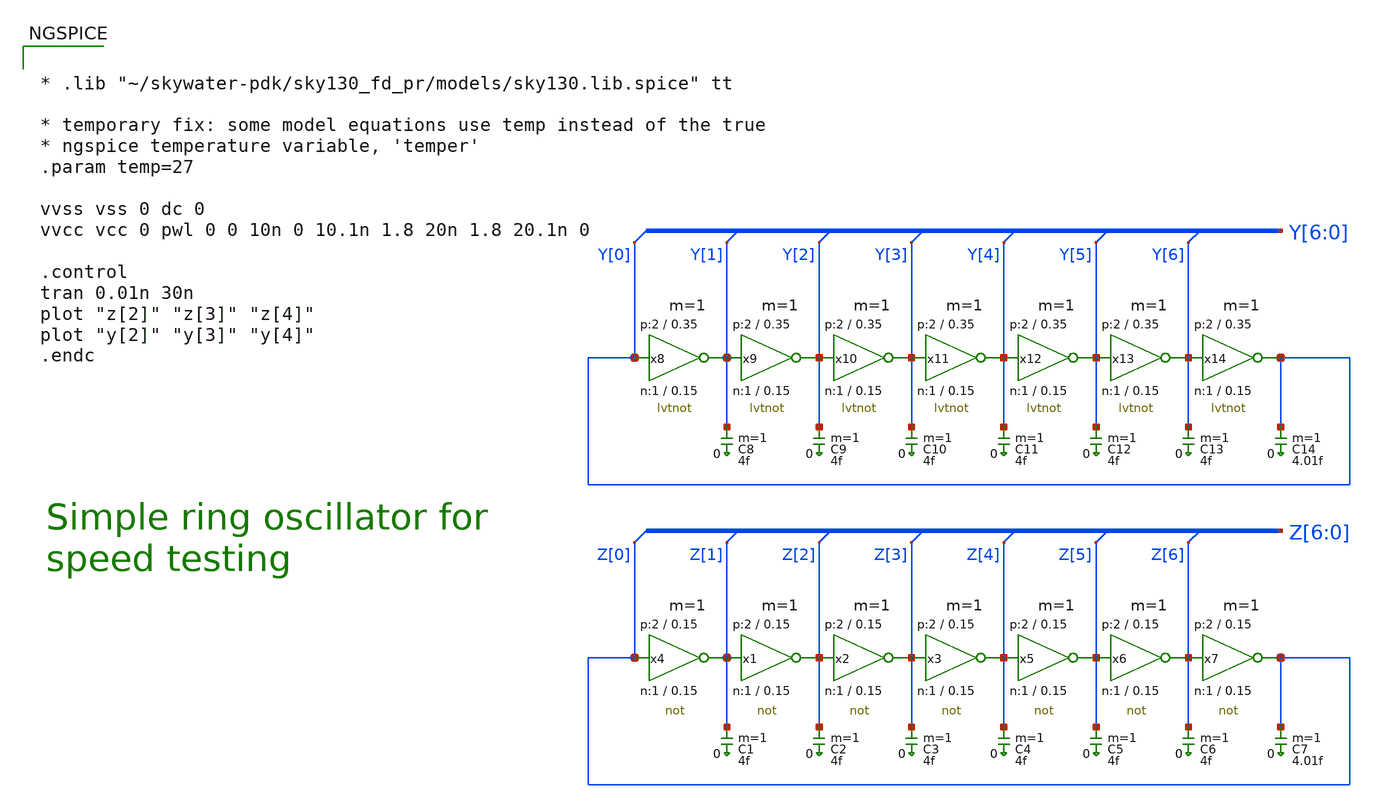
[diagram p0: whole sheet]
** sch_path: sky130_tests/test_inv.sch
* Copyright 2020 Stefan Frederik Schippers
* Licensed under the Apache License, Version 2.0 (the "License");
* you may not use this file except in compliance with the License.
* You may obtain a copy of the License at
* https://www.apache.org/licenses/LICENSE-2.0
* Unless required by applicable law or agreed to in writing, software
* distributed under the License is distributed on an "AS IS" BASIS,
* WITHOUT WARRANTIES OR CONDITIONS OF ANY KIND, either express or implied.
* See the License for the specific language governing permissions and
* limitations under the License.
**.subckt test_inv
x4 Z[1] Z[0] VCC VSS not W_N=1 L_N=0.15 W_P=2 L_P=0.15 m=1
C1 Z[1] 0 4f m=1
x1 Z[2] Z[1] VCC VSS not W_N=1 L_N=0.15 W_P=2 L_P=0.15 m=1
x2 Z[3] Z[2] VCC VSS not W_N=1 L_N=0.15 W_P=2 L_P=0.15 m=1
x3 Z[4] Z[3] VCC VSS not W_N=1 L_N=0.15 W_P=2 L_P=0.15 m=1
x5 Z[5] Z[4] VCC VSS not W_N=1 L_N=0.15 W_P=2 L_P=0.15 m=1
x6 Z[6] Z[5] VCC VSS not W_N=1 L_N=0.15 W_P=2 L_P=0.15 m=1
x7 Z[0] Z[6] VCC VSS not W_N=1 L_N=0.15 W_P=2 L_P=0.15 m=1
C2 Z[2] 0 4f m=1
C3 Z[3] 0 4f m=1
C4 Z[4] 0 4f m=1
C5 Z[5] 0 4f m=1
C6 Z[6] 0 4f m=1
C7 Z[0] 0 4.01f m=1
x8 Y[1] Y[0] VCC VSS lvtnot W_N=1 L_N=0.15 W_P=2 L_P=0.35 m=1
C8 Y[1] 0 4f m=1
x9 Y[2] Y[1] VCC VSS lvtnot W_N=1 L_N=0.15 W_P=2 L_P=0.35 m=1
x10 Y[3] Y[2] VCC VSS lvtnot W_N=1 L_N=0.15 W_P=2 L_P=0.35 m=1
x11 Y[4] Y[3] VCC VSS lvtnot W_N=1 L_N=0.15 W_P=2 L_P=0.35 m=1
x12 Y[5] Y[4] VCC VSS lvtnot W_N=1 L_N=0.15 W_P=2 L_P=0.35 m=1
x13 Y[6] Y[5] VCC VSS lvtnot W_N=1 L_N=0.15 W_P=2 L_P=0.35 m=1
x14 Y[0] Y[6] VCC VSS lvtnot W_N=1 L_N=0.15 W_P=2 L_P=0.35 m=1
C9 Y[2] 0 4f m=1
C10 Y[3] 0 4f m=1
C11 Y[4] 0 4f m=1
C12 Y[5] 0 4f m=1
C13 Y[6] 0 4f m=1
C14 Y[0] 0 4.01f m=1
**** begin user architecture code


* .lib "~/skywater-pdk/sky130_fd_pr/models/sky130.lib.spice" tt

* temporary fix: some model equations use temp instead of the true
* ngspice temperature variable, 'temper'
.param temp=27

vvss vss 0 dc 0
vvcc vcc 0 pwl 0 0 10n 0 10.1n 1.8 20n 1.8 20.1n 0

.control
tran 0.01n 30n
plot "z[2]" "z[3]" "z[4]"
plot "y[2]" "y[3]" "y[4]"
.endc


**** end user architecture code
**.ends
**** begin user architecture code

.include   ~/skywater-pdk/sky130_fd_pr_ngspice/cells/nfet_01v8/sky130_fd_pr__nfet_01v8__tt.corner.spice
.include ~/skywater-pdk/sky130_fd_pr_ngspice/cells/nfet_01v8_lvt/sky130_fd_pr__nfet_01v8_lvt__tt.corner.spice
.include ~/skywater-pdk/sky130_fd_pr_ngspice/cells/pfet_01v8/sky130_fd_pr__pfet_01v8__tt.corner.spice
.include ~/skywater-pdk/sky130_fd_pr_ngspice/cells/nfet_03v3_nvt/sky130_fd_pr__nfet_03v3_nvt__tt.corner.spice
.include ~/skywater-pdk/sky130_fd_pr_ngspice/cells/nfet_05v0_nvt/sky130_fd_pr__nfet_05v0_nvt__tt.corner.spice
.include ~/skywater-pdk/sky130_fd_pr_ngspice/cells/esd_nfet_01v8/sky130_fd_pr__esd_nfet_01v8__tt.corner.spice
.include ~/skywater-pdk/sky130_fd_pr_ngspice/cells/pfet_01v8_lvt/sky130_fd_pr__pfet_01v8_lvt__tt.corner.spice
.include ~/skywater-pdk/sky130_fd_pr_ngspice/cells/pfet_01v8_hvt/sky130_fd_pr__pfet_01v8_hvt__tt.corner.spice
.include ~/skywater-pdk/sky130_fd_pr_ngspice/cells/esd_pfet_g5v0d10v5/sky130_fd_pr__esd_pfet_g5v0d10v5__tt.corner.spice
.include ~/skywater-pdk/sky130_fd_pr_ngspice/cells/pfet_g5v0d10v5/sky130_fd_pr__pfet_g5v0d10v5__tt.corner.spice
.include ~/skywater-pdk/sky130_fd_pr_ngspice/cells/pfet_g5v0d16v0/sky130_fd_pr__pfet_g5v0d16v0__tt.corner.spice
.include ~/skywater-pdk/sky130_fd_pr_ngspice/cells/nfet_g5v0d10v5/sky130_fd_pr__nfet_g5v0d10v5__tt.corner.spice
.include ~/skywater-pdk/sky130_fd_pr_ngspice/cells/nfet_g5v0d16v0/sky130_fd_pr__nfet_g5v0d16v0__tt_discrete.corner.spice
.include ~/skywater-pdk/sky130_fd_pr_ngspice/cells/esd_nfet_g5v0d10v5/sky130_fd_pr__esd_nfet_g5v0d10v5__tt.corner.spice
.include ~/skywater-pdk/sky130_fd_pr_ngspice/models/corners/tt/nonfet.spice
* Mismatch parameters
.include ~/skywater-pdk/sky130_fd_pr_ngspice/cells/nfet_01v8/sky130_fd_pr__nfet_01v8__mismatch.corner.spice
.include ~/skywater-pdk/sky130_fd_pr_ngspice/cells/pfet_01v8/sky130_fd_pr__pfet_01v8__mismatch.corner.spice
.include ~/skywater-pdk/sky130_fd_pr_ngspice/cells/nfet_01v8_lvt/sky130_fd_pr__nfet_01v8_lvt__mismatch.corner.spice
.include ~/skywater-pdk/sky130_fd_pr_ngspice/cells/pfet_01v8_lvt/sky130_fd_pr__pfet_01v8_lvt__mismatch.corner.spice
.include ~/skywater-pdk/sky130_fd_pr_ngspice/cells/pfet_01v8_hvt/sky130_fd_pr__pfet_01v8_hvt__mismatch.corner.spice
.include ~/skywater-pdk/sky130_fd_pr_ngspice/cells/nfet_g5v0d10v5/sky130_fd_pr__nfet_g5v0d10v5__mismatch.corner.spice
.include ~/skywater-pdk/sky130_fd_pr_ngspice/cells/pfet_g5v0d10v5/sky130_fd_pr__pfet_g5v0d10v5__mismatch.corner.spice
.include ~/skywater-pdk/sky130_fd_pr_ngspice/cells/nfet_05v0_nvt/sky130_fd_pr__nfet_05v0_nvt__mismatch.corner.spice
.include ~/skywater-pdk/sky130_fd_pr_ngspice/cells/nfet_03v3_nvt/sky130_fd_pr__nfet_03v3_nvt__mismatch.corner.spice
* Resistor/Capacitor
.include ~/skywater-pdk/sky130_fd_pr_ngspice/models/r+c/res_typical__cap_typical.spice
.include ~/skywater-pdk/sky130_fd_pr_ngspice/models/r+c/res_typical__cap_typical__lin.spice
* Special cells
.include ~/skywater-pdk/sky130_fd_pr_ngspice/models/corners/tt/specialized_cells.spice
* All models
.include ~/skywater-pdk/sky130_fd_pr_ngspice/models/all.spice
* Corner
.include ~/skywater-pdk/sky130_fd_pr_ngspice/models/corners/tt/rf.spice


**** end user architecture code
.end
